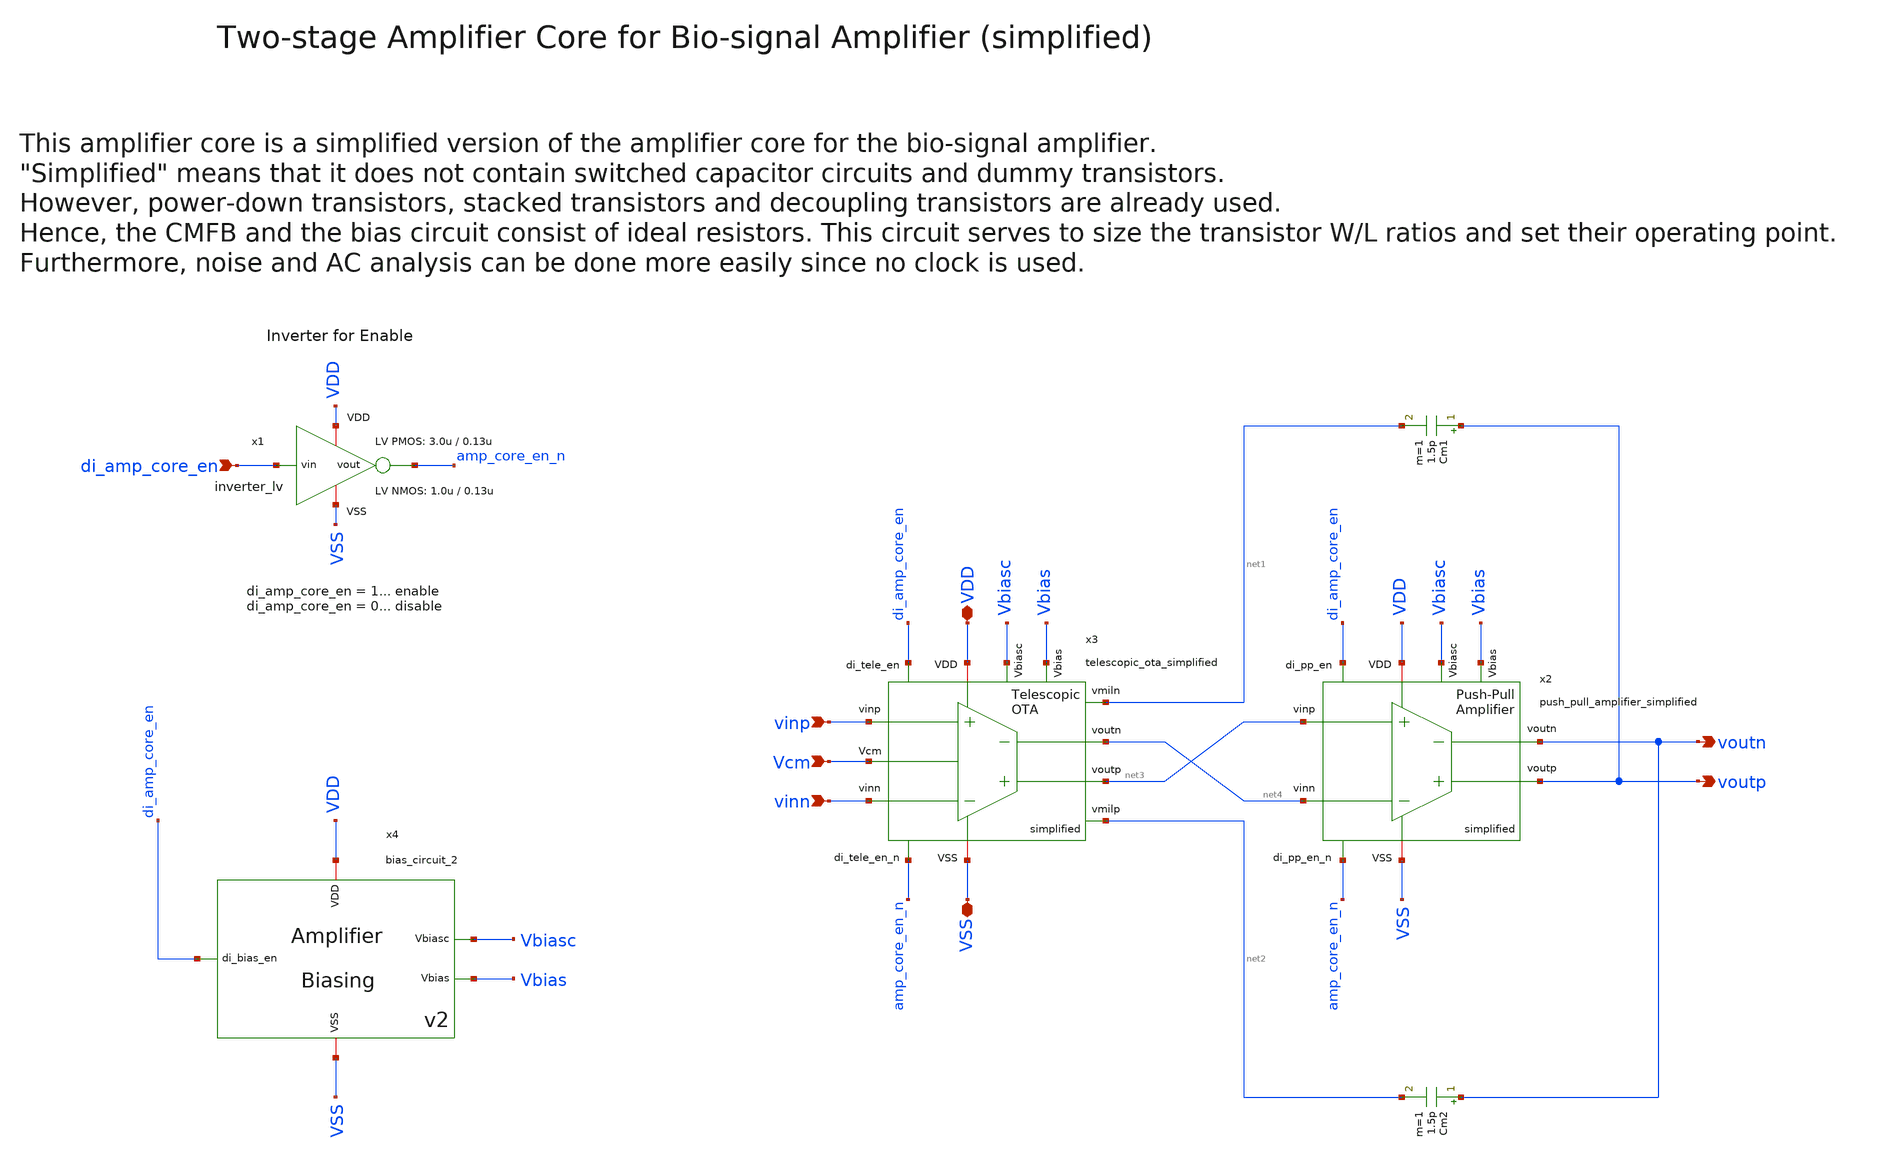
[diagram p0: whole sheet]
** sch_path: SG13G2_ATBS-ADC-main/xschem/bio_amplifier/amplifier_core/amplifier_core_simplified.sch
**.subckt amplifier_core_simplified VDD di_amp_core_en vinp vinn voutp voutn Vcm VSS
*.iopin VDD
*.ipin di_amp_core_en
*.ipin vinp
*.ipin vinn
*.opin voutp
*.opin voutn
*.ipin Vcm
*.iopin VSS
x1 VDD di_amp_core_en amp_core_en_n VSS inverter_lv W_P=3.0u L_P=0.13u W_N=1.0u L_N=0.13u
Cm1 voutp net1 1.5p m=1
Cm2 voutn net2 1.5p m=1
x2 VDD voutp voutn net4 net3 VSS amp_core_en_n di_amp_core_en Vbiasc Vbias
+ push_pull_amplifier_simplified
x3 net1 net2 net3 net4 VDD vinn vinp VSS Vcm di_amp_core_en amp_core_en_n Vbiasc Vbias
+ telescopic_ota_simplified
x4 di_amp_core_en Vbiasc VDD VSS Vbias bias_circuit_2
**.ends
.end
